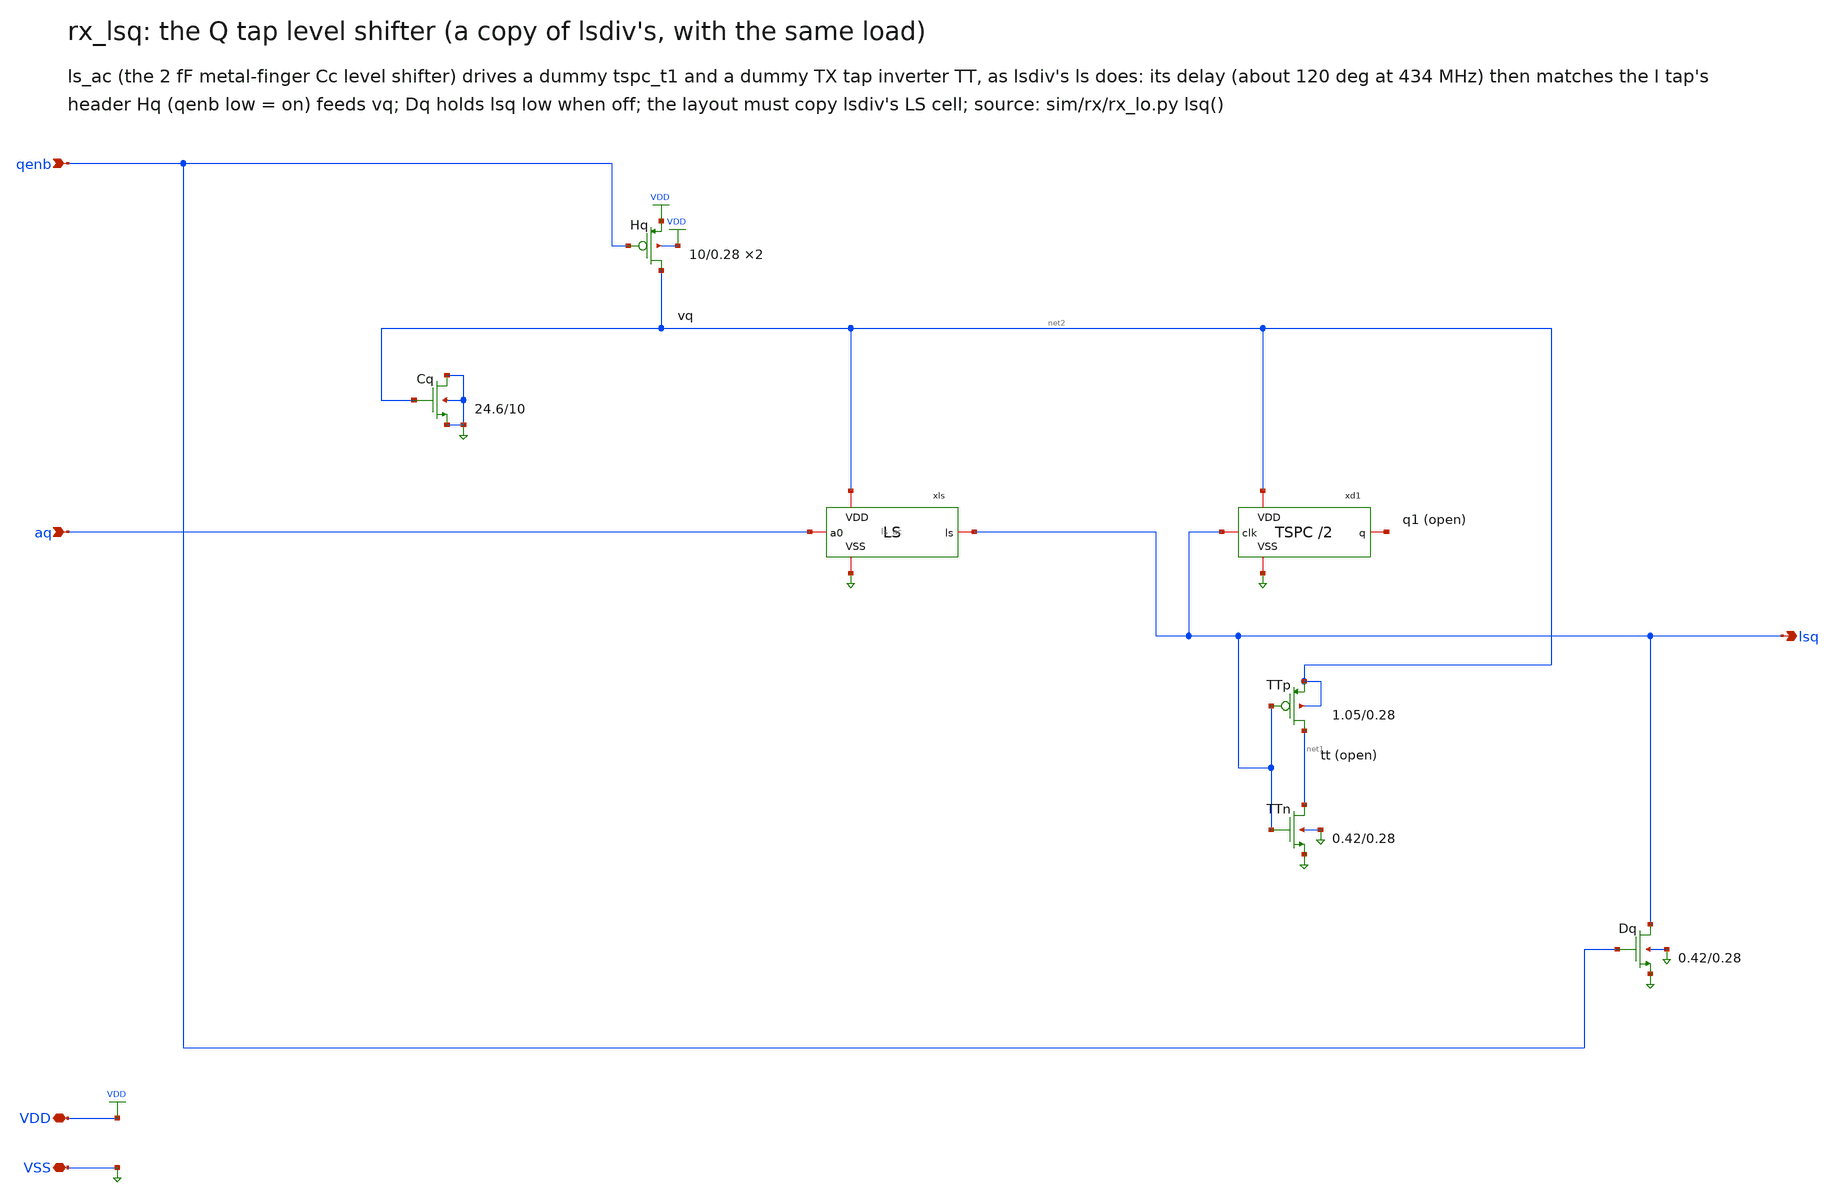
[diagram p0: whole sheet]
** sch_path: xschem/rx_lsq.sch
**.subckt rx_lsq VDD VSS aq qenb lsq
*.iopin VDD
*.iopin VSS
*.ipin aq
*.ipin qenb
*.opin lsq
XHq net2 qenb VDD VDD pfet_03v3 L=0.28u W=10.0u nf=1 ad=5.0p as=5.0p pd=21.0u ps=21.0u nrd=0 nrs=0
+ sa=0 sb=0 sd=0 m=2
XCq VSS net2 VSS VSS nfet_03v3 L=10.0u W=24.57u nf=1 ad=12.285p as=12.285p pd=50.14u ps=50.14u nrd=0
+ nrs=0 sa=0 sb=0 sd=0 m=1
xls net2 VSS aq lsq ls_ac
xd1 net2 VSS lsq net3 tspc_t1
XTTp net1 lsq net2 net2 pfet_03v3 L=0.28u W=1.0499999999999998u nf=1 ad=0.5249999999999999p
+ as=0.5249999999999999p pd=3.0999999999999996u ps=3.0999999999999996u nrd=0 nrs=0 sa=0 sb=0 sd=0 m=1
XTTn net1 lsq VSS VSS nfet_03v3 L=0.28u W=0.41999999999999993u nf=1 ad=0.20999999999999996p
+ as=0.20999999999999996p pd=1.8399999999999999u ps=1.8399999999999999u nrd=0 nrs=0 sa=0 sb=0 sd=0 m=1
XDq lsq qenb VSS VSS nfet_03v3 L=0.28u W=0.41999999999999993u nf=1 ad=0.20999999999999996p
+ as=0.20999999999999996p pd=1.8399999999999999u ps=1.8399999999999999u nrd=0 nrs=0 sa=0 sb=0 sd=0 m=1
**.ends

* expanding   symbol:  ls_ac.sym # of pins=4
** sym_path: xschem/ls_ac.sym
** sch_path: xschem/ls_ac.sch
.subckt ls_ac VDD VSS a0 ls
*.iopin VDD
*.iopin VSS
*.ipin a0
*.opin ls
XL1p net2 net1 VDD VDD pfet_03v3 L=0.28u W=0.5u nf=1 ad=0.25p as=0.25p pd=2.0u ps=2.0u nrd=0 nrs=0
+ sa=0 sb=0 sd=0 m=1
XL1n net2 net1 VSS VSS nfet_03v3 L=0.28u W=0.21999999999999997u nf=1 ad=0.10999999999999999p
+ as=0.10999999999999999p pd=1.44u ps=1.44u nrd=0 nrs=0 sa=0 sb=0 sd=0 m=1
XL2p net3 net2 VDD VDD pfet_03v3 L=0.28u W=1.5u nf=1 ad=0.75p as=0.75p pd=4.0u ps=4.0u nrd=0 nrs=0
+ sa=0 sb=0 sd=0 m=1
XL2n net3 net2 VSS VSS nfet_03v3 L=0.28u W=0.6u nf=1 ad=0.3p as=0.3p pd=2.2u ps=2.2u nrd=0 nrs=0
+ sa=0 sb=0 sd=0 m=1
XL3p ls net3 VDD VDD pfet_03v3 L=0.28u W=3.0u nf=1 ad=1.5p as=1.5p pd=7.0u ps=7.0u nrd=0 nrs=0 sa=0
+ sb=0 sd=0 m=1
XL3n ls net3 VSS VSS nfet_03v3 L=0.28u W=1.2u nf=1 ad=0.6p as=0.6p pd=3.4u ps=3.4u nrd=0 nrs=0 sa=0
+ sb=0 sd=0 m=1
Cc a0 net1 2e-15 m=1
XLRB net1 VSS net4 VDD pfet_03v3 L=2.0u W=0.21999999999999997u nf=1 ad=0.10999999999999999p
+ as=0.10999999999999999p pd=1.44u ps=1.44u nrd=0 nrs=0 sa=0 sb=0 sd=0 m=1
XR1 ls net4 VSS ppolyf_u_1k r_width=1.0e-6 r_length=159.125e-6 m=1
XC1 VSS net4 VSS VSS nfet_03v3 L=16.0u W=16.0u nf=1 ad=8.0p as=8.0p pd=33.0u ps=33.0u nrd=0 nrs=0
+ sa=0 sb=0 sd=0 m=1
.ends


* expanding   symbol:  tspc_t1.sym # of pins=4
** sym_path: xschem/tspc_t1.sym
** sch_path: xschem/tspc_t1.sch
.subckt tspc_t1 VDD VSS clk q
*.iopin VDD
*.iopin VSS
*.ipin clk
*.opin q
Xp1 net1 net6 VDD VDD pfet_03v3 L=0.28u W=2.0u nf=1 ad=1.0p as=1.0p pd=5.0u ps=5.0u nrd=0 nrs=0 sa=0
+ sb=0 sd=0 m=1
Xp2 net4 clk net1 VDD pfet_03v3 L=0.28u W=2.0u nf=1 ad=1.0p as=1.0p pd=5.0u ps=5.0u nrd=0 nrs=0 sa=0
+ sb=0 sd=0 m=1
Xn1 net4 net6 VSS VSS nfet_03v3 L=0.28u W=1.0u nf=1 ad=0.5p as=0.5p pd=3.0u ps=3.0u nrd=0 nrs=0 sa=0
+ sb=0 sd=0 m=1
Xp3 net5 clk VDD VDD pfet_03v3 L=0.28u W=2.0u nf=1 ad=1.0p as=1.0p pd=5.0u ps=5.0u nrd=0 nrs=0 sa=0
+ sb=0 sd=0 m=1
Xn2 net5 net4 net2 VSS nfet_03v3 L=0.28u W=1.0u nf=1 ad=0.5p as=0.5p pd=3.0u ps=3.0u nrd=0 nrs=0
+ sa=0 sb=0 sd=0 m=1
Xn3 net2 clk VSS VSS nfet_03v3 L=0.28u W=1.0u nf=1 ad=0.5p as=0.5p pd=3.0u ps=3.0u nrd=0 nrs=0 sa=0
+ sb=0 sd=0 m=1
Xp4 net6 net5 VDD VDD pfet_03v3 L=0.28u W=2.0u nf=1 ad=1.0p as=1.0p pd=5.0u ps=5.0u nrd=0 nrs=0 sa=0
+ sb=0 sd=0 m=1
Xn4 net6 clk net3 VSS nfet_03v3 L=0.28u W=1.0u nf=1 ad=0.5p as=0.5p pd=3.0u ps=3.0u nrd=0 nrs=0 sa=0
+ sb=0 sd=0 m=1
Xn5 net3 net5 VSS VSS nfet_03v3 L=0.28u W=1.0u nf=1 ad=0.5p as=0.5p pd=3.0u ps=3.0u nrd=0 nrs=0 sa=0
+ sb=0 sd=0 m=1
Xqp q net6 VDD VDD pfet_03v3 L=0.28u W=1.5u nf=1 ad=0.75p as=0.75p pd=4.0u ps=4.0u nrd=0 nrs=0 sa=0
+ sb=0 sd=0 m=1
Xqn q net6 VSS VSS nfet_03v3 L=0.28u W=0.6u nf=1 ad=0.3p as=0.3p pd=2.2u ps=2.2u nrd=0 nrs=0 sa=0
+ sb=0 sd=0 m=1
.ends

.end
